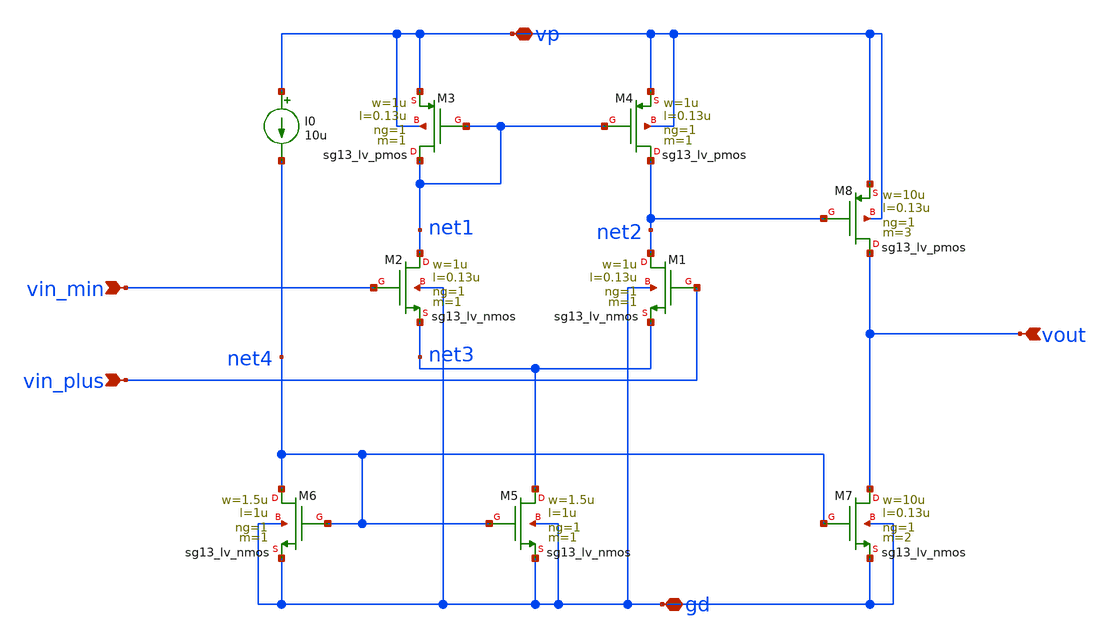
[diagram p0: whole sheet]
** sch_path: charge_pump/old_sch/amp_sz.sch
**.subckt amp_sz vin_min vin_plus vout gd vp
*.ipin vin_min
*.ipin vin_plus
*.ipin vout
*.iopin gd
*.iopin vp
XM1 net2 vin_plus net3 gd sg13_lv_nmos w=1u l=0.13u ng=1 m=1 mm_ok=1
XM2 net1 vin_min net3 gd sg13_lv_nmos w=1u l=0.13u ng=1 m=1 mm_ok=1
XM3 net1 net1 vp vp sg13_lv_pmos w=1u l=0.13u ng=1 m=1 mm_ok=1
XM4 net2 net1 vp vp sg13_lv_pmos w=1u l=0.13u ng=1 m=1 mm_ok=1
I0 vp net4 10u
XM5 net3 net4 gd gd sg13_lv_nmos w=1.5u l=1u ng=1 m=1 mm_ok=1
XM6 net4 net4 gd gd sg13_lv_nmos w=1.5u l=1u ng=1 m=1 mm_ok=1
XM7 vout net4 gd gd sg13_lv_nmos w=10u l=0.13u ng=1 m=2 mm_ok=1
XM8 vout net2 vp vp sg13_lv_pmos w=10u l=0.13u ng=1 m=3 mm_ok=1
**.ends
.end
